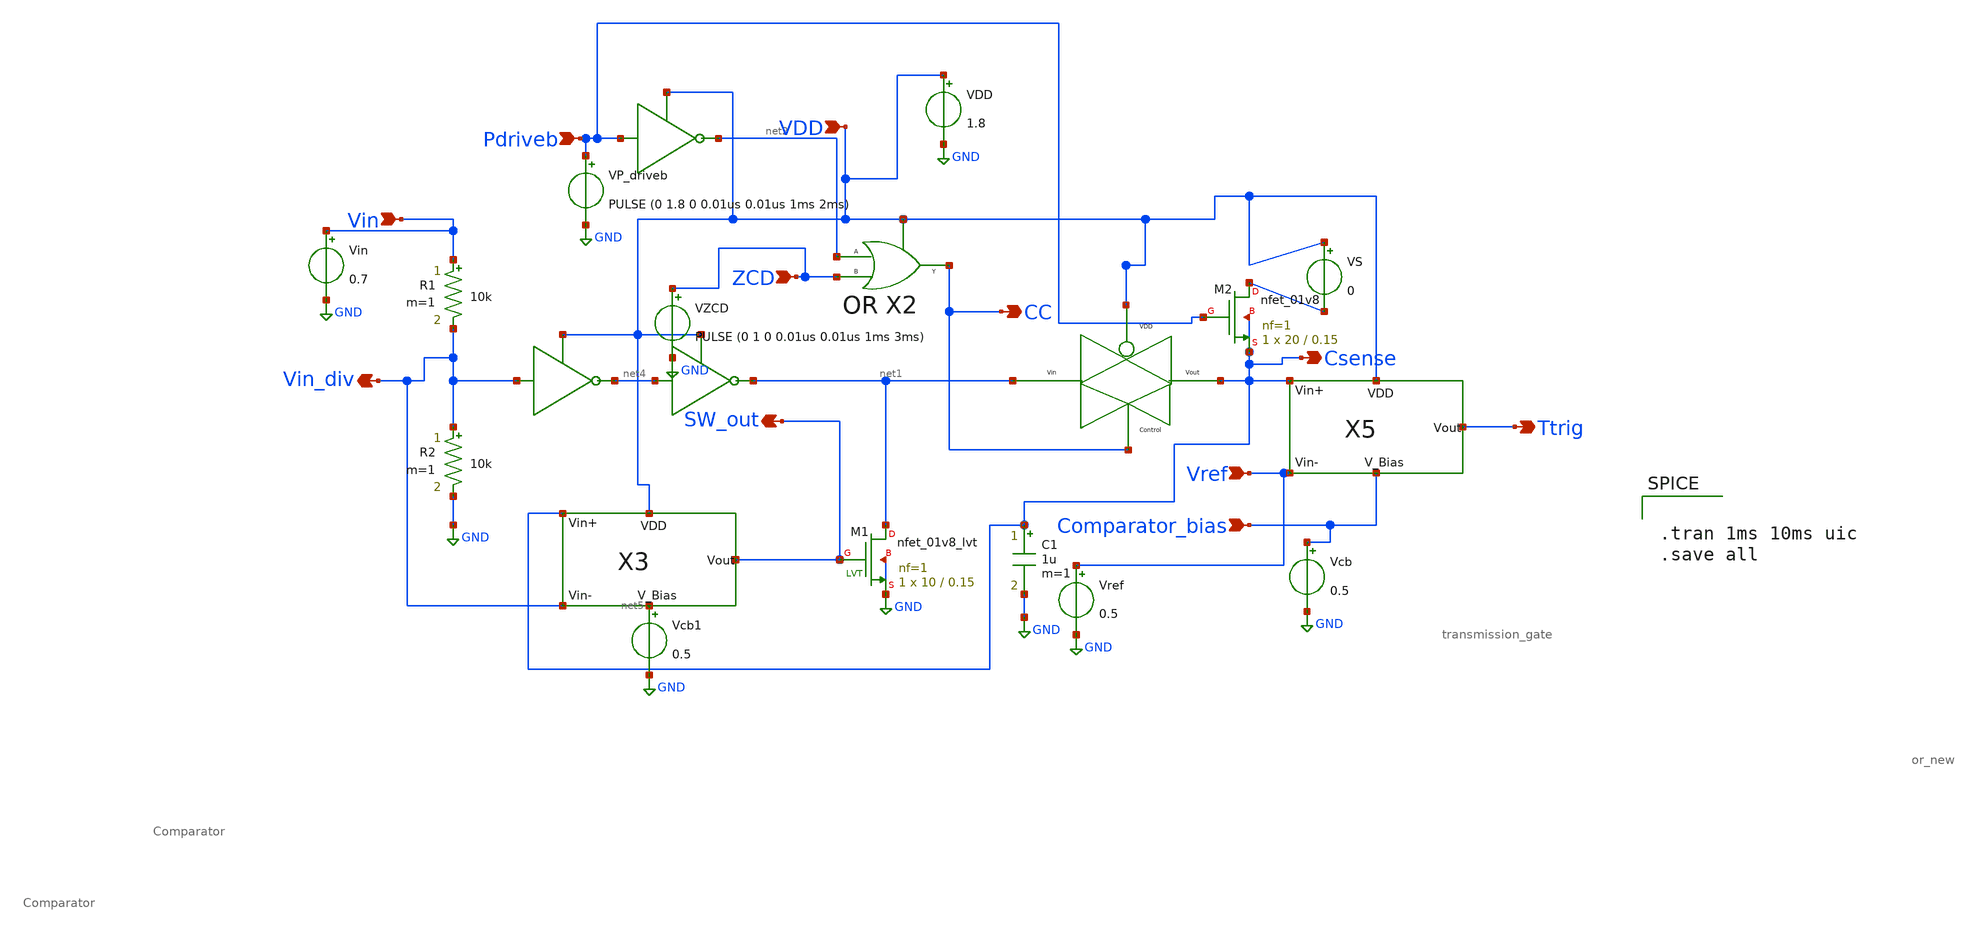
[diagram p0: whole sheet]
** sch_path: Current Sensor/otg_deep.sch
**.subckt otg_deep Vref Vin_div Comparator_bias Pdriveb ZCD Vin Ttrig VDD Csense SW_out CC
*.ipin Vref
*.opin Vin_div
*.ipin Comparator_bias
*.ipin Pdriveb
*.ipin ZCD
*.ipin Vin
*.opin Ttrig
*.ipin VDD
*.opin Csense
*.opin SW_out
*.opin CC
Vin Vin GND 0.7
Vref Vref GND 0.5
VDD VDD GND 1.8
Vcb Comparator_bias GND 0.5
VP_driveb Pdriveb GND PULSE (0 1.8 0 0.01us 0.01us 1ms 2ms)
VZCD ZCD GND PULSE (0 1 0 0.01us 0.01us 1ms 3ms)
X1 net1 Csense CC VDD transmission_gate
X5 Comparator_bias Csense Vref Ttrig VDD Comparator
R1 Vin Vin_div 10k m=1
R2 Vin_div GND 10k m=1
C1 Csense GND 1u m=1
X2 ZCD net2 CC VDD or_new
XM1 net1 SW_out GND GND sky130_fd_pr__nfet_01v8_lvt L=0.15 W=10 nf=1 ad='int((nf+1)/2) * W/nf * 0.29'
+ as='int((nf+2)/2) * W/nf * 0.29' pd='2*int((nf+1)/2) * (W/nf + 0.29)' ps='2*int((nf+2)/2) * (W/nf + 0.29)'
+ nrd='0.29 / W' nrs='0.29 / W' sa=0 sb=0 sd=0 mult=1 m=1
VS VDD net3 0
XM2 net3 Pdriveb Csense Csense sky130_fd_pr__nfet_01v8 L=0.15 W=20 nf=1 ad='int((nf+1)/2) * W/nf * 0.29'
+ as='int((nf+2)/2) * W/nf * 0.29' pd='2*int((nf+1)/2) * (W/nf + 0.29)' ps='2*int((nf+2)/2) * (W/nf + 0.29)'
+ nrd='0.29 / W' nrs='0.29 / W' sa=0 sb=0 sd=0 mult=1 m=1
X3 net5 Csense Vin_div SW_out VDD Comparator
Vcb1 net5 GND 0.5
**** begin user architecture code


.tran 1ms 10ms uic
.save all


** opencircuitdesign pdks install
.lib $::SKYWATER_MODELS/sky130.lib.spice tt_mm


**** end user architecture code
**.ends
.GLOBAL GND
.end
